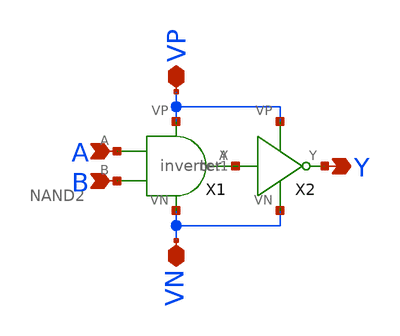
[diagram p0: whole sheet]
** sch_path: mp1/AND2.sch
**.subckt AND2 A B VP VN Y
*.ipin A
*.ipin B
*.iopin VP
*.iopin VN
*.opin Y
X1 A net1 VP VN B NAND2
X2 net1 Y VP VN inverter
**.ends

* expanding   symbol:  /home/jacob/madvlsi/mp1/NAND2.sym # of pins=5
** sym_path: mp1/NAND2.sym
** sch_path: mp1/NAND2.sch
.subckt NAND2 A Y VP VN B
*.iopin VP
*.iopin VN
*.ipin A
*.ipin B
*.opin Y
XM1 Y A VP VP sky130_fd_pr__pfet_01v8 L=0.15 W=1 nf=1 ad='int((nf+1)/2) * W/nf * 0.29' as='int((nf+2)/2) * W/nf * 0.29'
+ pd='2*int((nf+1)/2) * (W/nf + 0.29)' ps='2*int((nf+2)/2) * (W/nf + 0.29)' nrd='0.29 / W' nrs='0.29 / W'
+ sa=0 sb=0 sd=0 mult=1 m=1
XM2 Y B VP VP sky130_fd_pr__pfet_01v8 L=0.15 W=1 nf=1 ad='int((nf+1)/2) * W/nf * 0.29' as='int((nf+2)/2) * W/nf * 0.29'
+ pd='2*int((nf+1)/2) * (W/nf + 0.29)' ps='2*int((nf+2)/2) * (W/nf + 0.29)' nrd='0.29 / W' nrs='0.29 / W'
+ sa=0 sb=0 sd=0 mult=1 m=1
XM3 Y A net1 VN sky130_fd_pr__nfet_01v8 L=0.15 W=1 nf=1 ad='int((nf+1)/2) * W/nf * 0.29' as='int((nf+2)/2) * W/nf * 0.29'
+ pd='2*int((nf+1)/2) * (W/nf + 0.29)' ps='2*int((nf+2)/2) * (W/nf + 0.29)' nrd='0.29 / W' nrs='0.29 / W'
+ sa=0 sb=0 sd=0 mult=1 m=1
XM4 net1 B VN VN sky130_fd_pr__nfet_01v8 L=0.15 W=1 nf=1 ad='int((nf+1)/2) * W/nf * 0.29' as='int((nf+2)/2) * W/nf * 0.29'
+ pd='2*int((nf+1)/2) * (W/nf + 0.29)' ps='2*int((nf+2)/2) * (W/nf + 0.29)' nrd='0.29 / W' nrs='0.29 / W'
+ sa=0 sb=0 sd=0 mult=1 m=1
.ends


* expanding   symbol:  /home/jacob/madvlsi/mp1/inverter.sym # of pins=4
** sym_path: mp1/inverter.sym
** sch_path: mp1/inverter.sch
.subckt inverter A Y VP VN
*.ipin A
*.iopin VP
*.iopin VN
*.opin Y
XM1 Y A VP VP sky130_fd_pr__pfet_01v8 L=0.15 W=1 nf=1 ad='int((nf+1)/2) * W/nf * 0.29' as='int((nf+2)/2) * W/nf * 0.29'
+ pd='2*int((nf+1)/2) * (W/nf + 0.29)' ps='2*int((nf+2)/2) * (W/nf + 0.29)' nrd='0.29 / W' nrs='0.29 / W'
+ sa=0 sb=0 sd=0 mult=1 m=1
XM2 Y A VN VN sky130_fd_pr__nfet_01v8 L=0.15 W=1 nf=1 ad='int((nf+1)/2) * W/nf * 0.29' as='int((nf+2)/2) * W/nf * 0.29'
+ pd='2*int((nf+1)/2) * (W/nf + 0.29)' ps='2*int((nf+2)/2) * (W/nf + 0.29)' nrd='0.29 / W' nrs='0.29 / W'
+ sa=0 sb=0 sd=0 mult=1 m=1
.ends

.end
